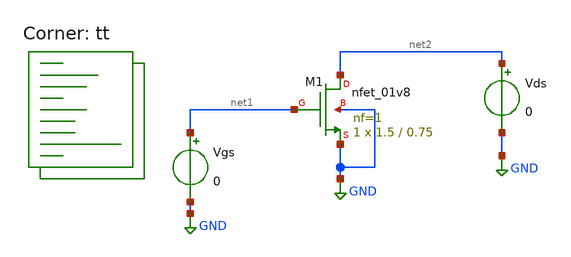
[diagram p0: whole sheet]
** sch_path: nmos_test.sch
**.subckt nmos_test
XM1 net2 net1 GND GND sky130_fd_pr__nfet_01v8 L=0.75 W=1.5 nf=1 ad='int((nf+1)/2) * W/nf * 0.29' as='int((nf+2)/2) * W/nf * 0.29'
+ pd='2*int((nf+1)/2) * (W/nf + 0.29)' ps='2*int((nf+2)/2) * (W/nf + 0.29)' nrd='0.29 / W' nrs='0.29 / W'
+ sa=0 sb=0 sd=0 mult=1 m=1
Vgs net1 GND 0
Vds net2 GND 0
**** begin user architecture code
.lib $::SKYWATER_MODELS/sky130.lib.spice tt



.save all
.dc Vds 0 1.8 0.0001 Vgs 0 1.8 0.3

.end

**** end user architecture code
**.ends
.GLOBAL GND
.end
